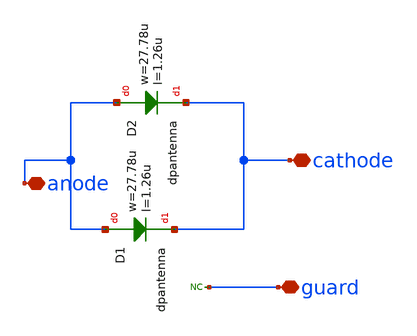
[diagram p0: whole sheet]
** sch_path: ihp-sg13g2/libs.ref/sg13g2_io/xschem/sg13g2_DCPDiode.sch
**.subckt sg13g2_DCPDiode cathode anode guard
*.iopin cathode
*.iopin anode
*.iopin guard
XD1 anode cathode dpantenna l=1.26u w=27.78u
XD2 anode cathode dpantenna l=1.26u w=27.78u
* noconn guard
**.ends
.end
